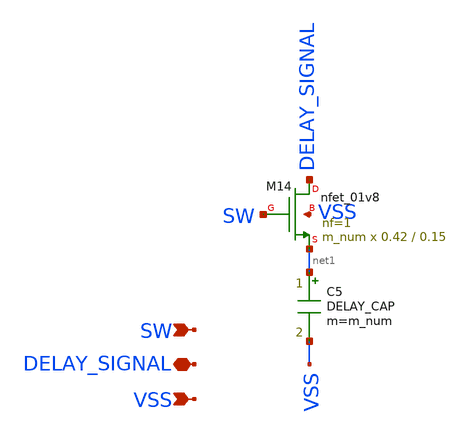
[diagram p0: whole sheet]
** sch_path: hgu/xschem/hgu_sw_cap.sch
**.subckt hgu_sw_cap SW VSS DELAY_SIGNAL
*.ipin SW
*.ipin VSS
*.iopin DELAY_SIGNAL
C5 net1 VSS DELAY_CAP m=m_num
XM14 DELAY_SIGNAL SW net1 VSS sky130_fd_pr__nfet_01v8 L=0.15 W=0.42 nf=1 ad='int((nf+1)/2) * W/nf * 0.29'
+ as='int((nf+2)/2) * W/nf * 0.29' pd='2*int((nf+1)/2) * (W/nf + 0.29)' ps='2*int((nf+2)/2) * (W/nf + 0.29)'
+ nrd='0.29 / W' nrs='0.29 / W' sa=0 sb=0 sd=0 mult=m_num m=m_num
**.ends
.end
